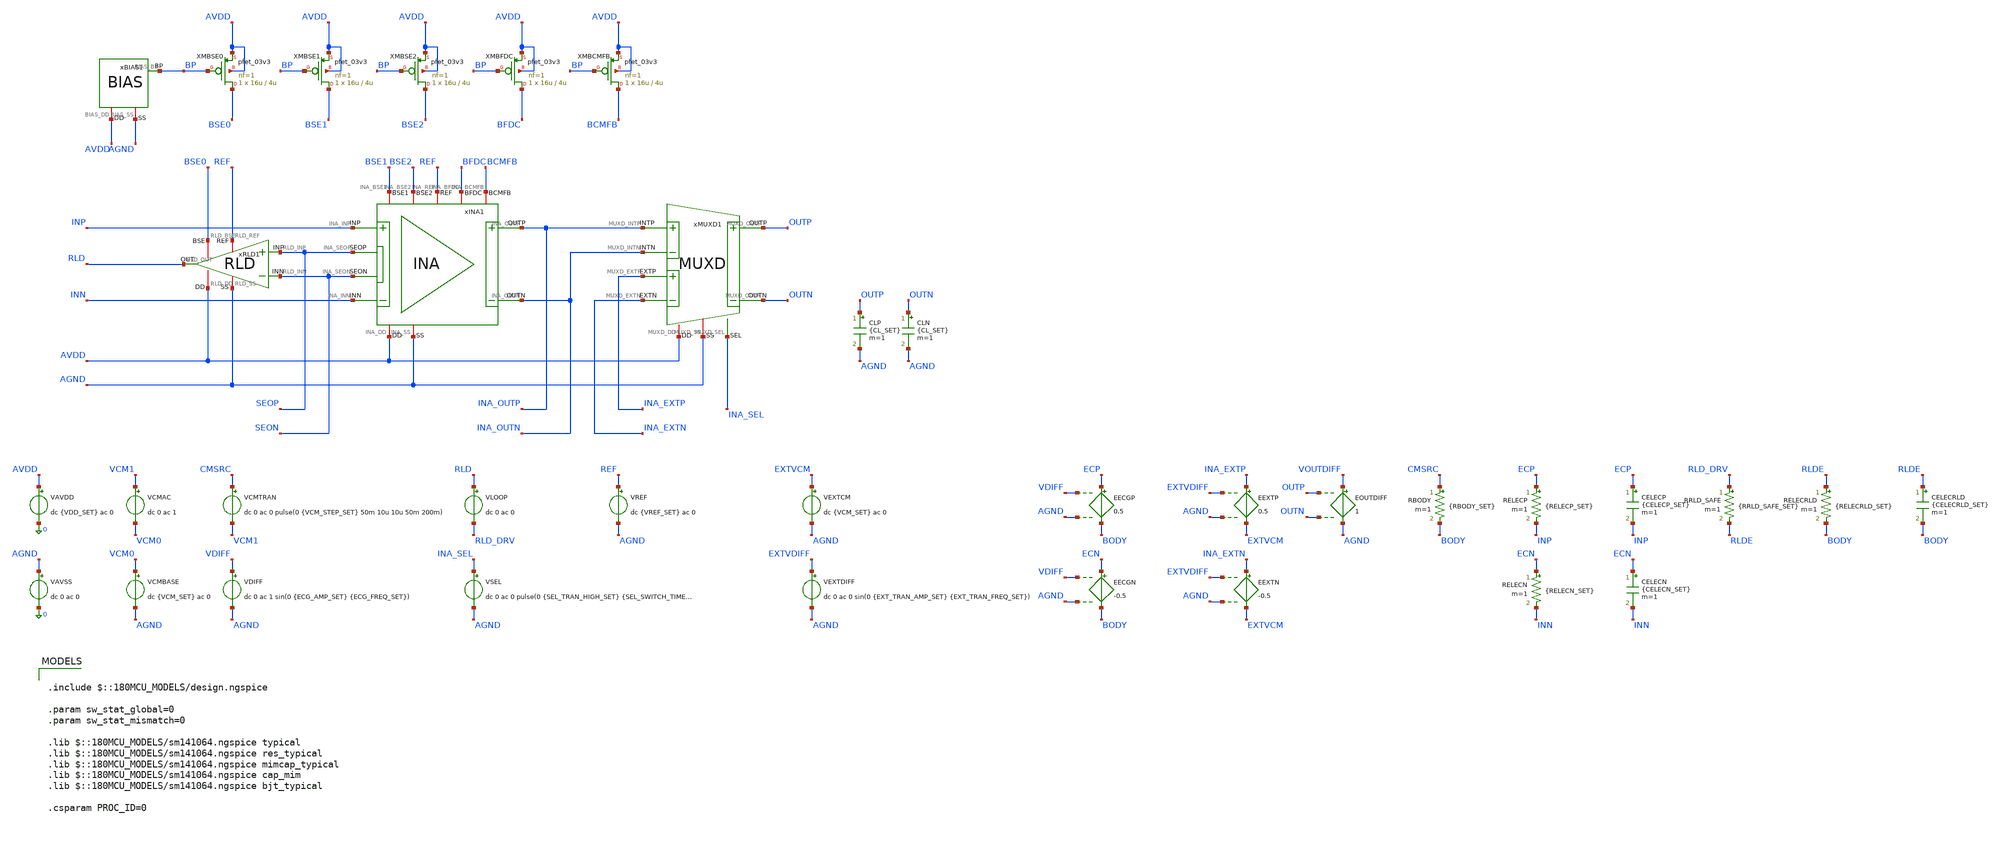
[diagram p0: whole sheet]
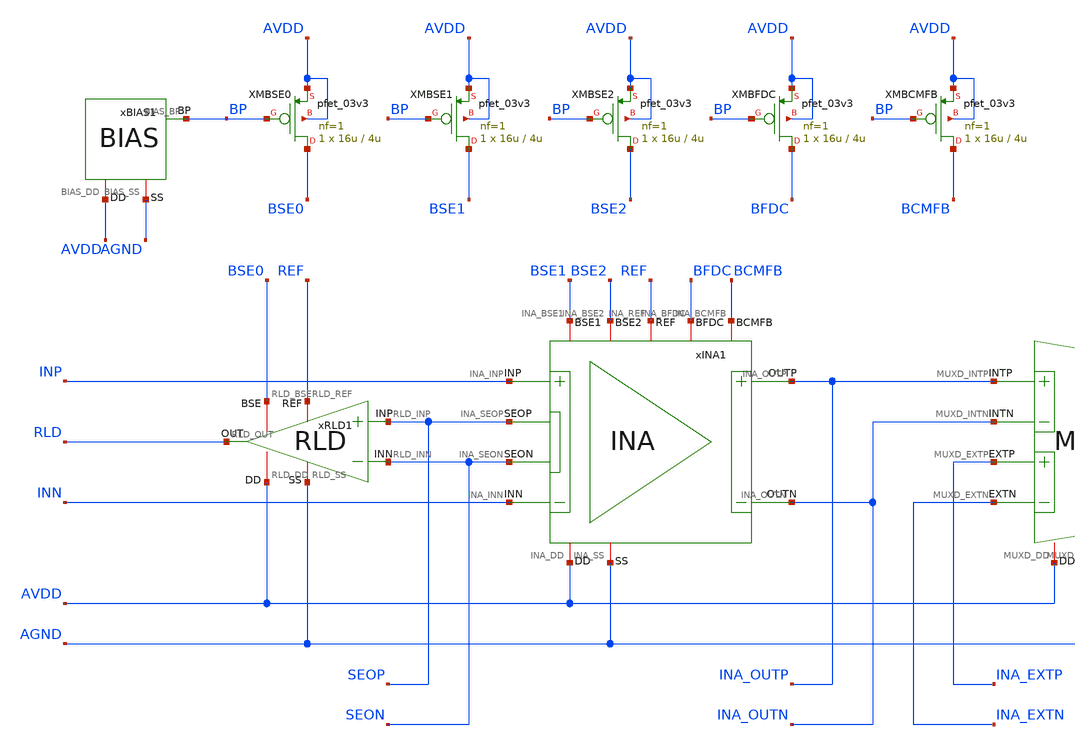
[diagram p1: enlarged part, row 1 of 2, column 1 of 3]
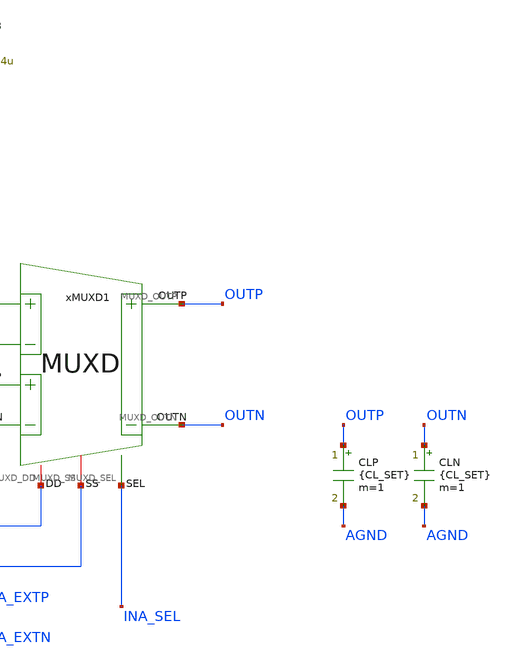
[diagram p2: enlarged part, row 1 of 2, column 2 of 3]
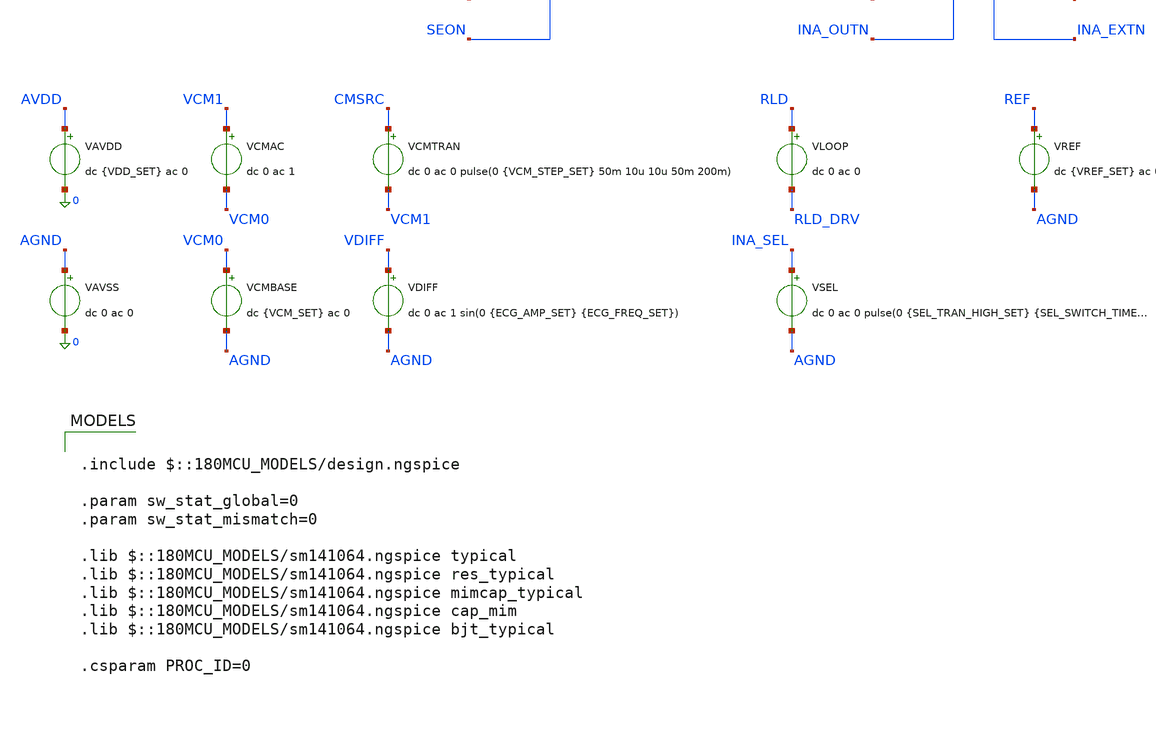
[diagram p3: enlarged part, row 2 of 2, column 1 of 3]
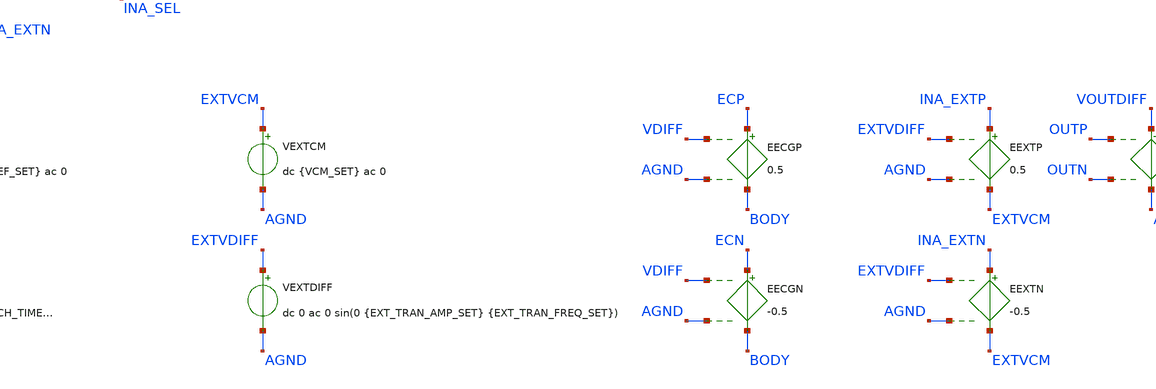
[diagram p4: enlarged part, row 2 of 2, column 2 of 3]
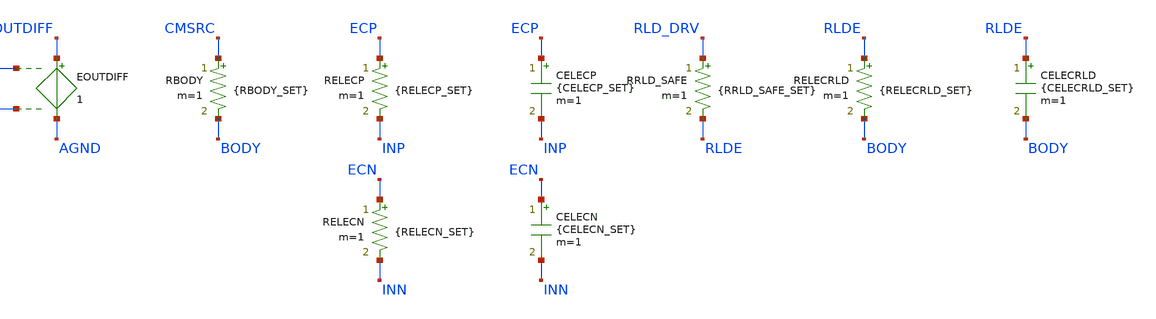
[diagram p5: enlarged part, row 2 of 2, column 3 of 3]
** sch_path: Design_Files/IC Design/Testbench/AFE_BLOCKS/INA_RLD/INA_RLD_TB_NOM.sch
**.subckt INA_RLD_TB_NOM
xMUXD1 AVDD AGND INA_OUTP INA_OUTN OUTN OUTP INA_EXTP INA_EXTN INA_SEL MUXD
xINA1 AVDD AGND INP INN INA_OUTN BFDC INA_OUTP BCMFB REF SEON SEOP BSE1 BSE2 INA
xRLD1 AVDD AGND SEOP SEON RLD REF BSE0 RLD
CLP OUTP AGND {CL_SET} m=1
CLN OUTN AGND {CL_SET} m=1
xBIAS1 AVDD AGND BP BIAS
XMBSE0 BSE0 BP AVDD AVDD pfet_03v3 L=4u W=16u nf=1 ad='int((nf+1)/2) * W/nf * 0.18u' as='int((nf+2)/2) * W/nf * 0.18u'
+ pd='2*int((nf+1)/2) * (W/nf + 0.18u)' ps='2*int((nf+2)/2) * (W/nf + 0.18u)' nrd='0.18u / W' nrs='0.18u / W'
+ sa=0 sb=0 sd=0 m=1
XMBSE1 BSE1 BP AVDD AVDD pfet_03v3 L=4u W=16u nf=1 ad='int((nf+1)/2) * W/nf * 0.18u' as='int((nf+2)/2) * W/nf * 0.18u'
+ pd='2*int((nf+1)/2) * (W/nf + 0.18u)' ps='2*int((nf+2)/2) * (W/nf + 0.18u)' nrd='0.18u / W' nrs='0.18u / W'
+ sa=0 sb=0 sd=0 m=1
XMBSE2 BSE2 BP AVDD AVDD pfet_03v3 L=4u W=16u nf=1 ad='int((nf+1)/2) * W/nf * 0.18u' as='int((nf+2)/2) * W/nf * 0.18u'
+ pd='2*int((nf+1)/2) * (W/nf + 0.18u)' ps='2*int((nf+2)/2) * (W/nf + 0.18u)' nrd='0.18u / W' nrs='0.18u / W'
+ sa=0 sb=0 sd=0 m=1
XMBFDC BFDC BP AVDD AVDD pfet_03v3 L=4u W=16u nf=1 ad='int((nf+1)/2) * W/nf * 0.18u' as='int((nf+2)/2) * W/nf * 0.18u'
+ pd='2*int((nf+1)/2) * (W/nf + 0.18u)' ps='2*int((nf+2)/2) * (W/nf + 0.18u)' nrd='0.18u / W' nrs='0.18u / W'
+ sa=0 sb=0 sd=0 m=1
XMBCMFB BCMFB BP AVDD AVDD pfet_03v3 L=4u W=16u nf=1 ad='int((nf+1)/2) * W/nf * 0.18u' as='int((nf+2)/2) * W/nf * 0.18u'
+ pd='2*int((nf+1)/2) * (W/nf + 0.18u)' ps='2*int((nf+2)/2) * (W/nf + 0.18u)' nrd='0.18u / W' nrs='0.18u / W'
+ sa=0 sb=0 sd=0 m=1
VAVDD AVDD 0 dc {VDD_SET} ac 0
.save i(vavdd)
VCMBASE VCM0 AGND dc {VCM_SET} ac 0
VCMAC VCM1 VCM0 dc 0 ac 1
VAVSS AGND 0 dc 0 ac 0
VCMTRAN CMSRC VCM1 dc 0 ac 0 pulse(0 {VCM_STEP_SET} 50m 10u 10u 50m 200m)
EECGP ECP BODY VDIFF AGND 0.5
EECGN ECN BODY VDIFF AGND -0.5
EEXTP INA_EXTP EXTVCM EXTVDIFF AGND 0.5
VDIFF VDIFF AGND dc 0 ac 1 sin(0 {ECG_AMP_SET} {ECG_FREQ_SET})
VLOOP RLD RLD_DRV dc 0 ac 0
.save i(vloop)
VSEL INA_SEL AGND dc 0 ac 0 pulse(0 {SEL_TRAN_HIGH_SET} {SEL_SWITCH_TIME_SET} 1u 1u 400m 800m)
VEXTCM EXTVCM AGND dc {VCM_SET} ac 0
VEXTDIFF EXTVDIFF AGND dc 0 ac 0 sin(0 {EXT_TRAN_AMP_SET} {EXT_TRAN_FREQ_SET})
EEXTN INA_EXTN EXTVCM EXTVDIFF AGND -0.5
EOUTDIFF VOUTDIFF AGND OUTP OUTN 1
RBODY CMSRC BODY {RBODY_SET} m=1
RELECP ECP INP {RELECP_SET} m=1
RELECN ECN INN {RELECN_SET} m=1
CELECP ECP INP {CELECP_SET} m=1
CELECN ECN INN {CELECN_SET} m=1
RRLD_SAFE RLD_DRV RLDE {RRLD_SAFE_SET} m=1
RELECRLD RLDE BODY {RELECRLD_SET} m=1
CELECRLD RLDE BODY {CELECRLD_SET} m=1
VREF REF AGND dc {VREF_SET} ac 0
.save i(vref)
**** begin user architecture code

.include $::180MCU_MODELS/design.ngspice

.param sw_stat_global=0
.param sw_stat_mismatch=0

.lib $::180MCU_MODELS/sm141064.ngspice typical
.lib $::180MCU_MODELS/sm141064.ngspice res_typical
.lib $::180MCU_MODELS/sm141064.ngspice mimcap_typical
.lib $::180MCU_MODELS/sm141064.ngspice cap_mim
.lib $::180MCU_MODELS/sm141064.ngspice bjt_typical

.csparam PROC_ID=0



.param VDD_SET=3.3
.param TEMP_SET=27
.param VCM_SET={VDD_SET/2}
.param VREF_SET={VDD_SET/2}

.param CL_SET=10p

.param ECG_AMP_SET=0.5m
.param ECG_FREQ_SET=10
.param VCM_STEP_SET=300m

.param RBODY_SET=100Meg

.param RELECP_SET=100k
.param RELECN_SET=100k
.param CELECP_SET=100n
.param CELECN_SET=100n

.param RRLD_SAFE_SET=1Meg
.param RELECRLD_SET=100k
.param CELECRLD_SET=100n

.param SEL_TRAN_HIGH_SET=0
.param SEL_SWITCH_TIME_SET=200m
.param EXT_TRAN_AMP_SET=0
.param EXT_TRAN_FREQ_SET=25

.csparam MC_RUNS=200

.temp {TEMP_SET}

.options gmin=1e-12
.options rshunt=1e12
.options method=gear





.control

destroy all

set noaskquit
set wr_singlescale
unset wr_vecnames

option klu
option numdgt=15
option method=gear
option maxord=2
option plotwinsize=0

if $&PROC_ID = 0
set proc=NOM
else
if $&PROC_ID = 1
set proc=FF
else
if $&PROC_ID = 2
set proc=SS
else
if $&PROC_ID = 3
set proc=FS
else
set proc=SF
end
end
end
end

shell mkdir -p /foss/designs/ECG_Acquisition_IC/Measurement_Results/IC_Simulation/AFE_BLOCKS/INA_RLD/{$proc}.Result_txt
shell rm -f /foss/designs/ECG_Acquisition_IC/Measurement_Results/IC_Simulation/AFE_BLOCKS/INA_RLD/{$proc}.Result_txt/{$proc}.*.txt

foreach vddval 3.3 3.0 3.6
foreach tval 27 -40 125

if $vddval = 3.3
if $tval = 27
set env=nom
else
if $tval = -40
set env=tl
else
set env=th
end
end
else
if $vddval = 3.0
if $tval = 27
set env=vl
else
if $tval = -40
set env=vltl
else
set env=vlth
end
end
else
if $tval = 27
set env=vh
else
if $tval = -40
set env=vhtl
else
set env=vhth
end
end
end
end

alterparam VDD_SET=$vddval
alterparam TEMP_SET=$tval

reset

save all
save @m.xmbse0.m0[id]
save @m.xmbse1.m0[id]
save @m.xmbse2.m0[id]
save @m.xmbfdc.m0[id]
save @m.xmbcmfb.m0[id]

foreach emode 0 1

if $emode = 0
set elec=bal
alter RELECP 100k
alter RELECN 100k
alter CELECP 100n
alter CELECN 100n
else
set elec=mis
alter RELECP 100k
alter RELECN 200k
alter CELECP 100n
alter CELECN 50n
end


* OFFSET

alter RRLD_SAFE 1Meg
alter @VSEL[DC]=0
alter @VDIFF[DC]=0

alter @VDIFF[ACMAG]=0
alter @VCMAC[ACMAG]=0
alter @VLOOP[ACMAG]=0
alter @VEXTDIFF[ACMAG]=0
alter @VREF[ACMAG]=0
alter @VAVDD[ACMAG]=0
alter @VAVSS[ACMAG]=0

dc VDIFF -10m 10m 10u

let ina_out_diff=v(INA_OUTP)-v(INA_OUTN)

meas dc vos_meas when ina_out_diff=0 cross=1

set vos_val=$&vos_meas

echo $vos_val > /foss/designs/ECG_Acquisition_IC/Measurement_Results/IC_Simulation/AFE_BLOCKS/INA_RLD/{$proc}.Result_txt/{$proc}.vos_{$env}_{$elec}.txt

destroy all

alter @VDIFF[DC]=$vos_val


* OP

alter RRLD_SAFE 1Meg
alter @VSEL[DC]=0

alter @VDIFF[ACMAG]=0
alter @VCMAC[ACMAG]=0
alter @VLOOP[ACMAG]=0
alter @VEXTDIFF[ACMAG]=0
alter @VREF[ACMAG]=0
alter @VAVDD[ACMAG]=0
alter @VAVSS[ACMAG]=0

op

let vin_cm=0.5*(v(INP)+v(INN))-v(AGND)
let vin_diff=v(INP)-v(INN)
let se_cm=0.5*(v(SEOP)+v(SEON))-v(AGND)
let se_diff=v(SEOP)-v(SEON)
let ina_out_cm=0.5*(v(INA_OUTP)+v(INA_OUTN))-v(AGND)
let ina_out_diff=v(INA_OUTP)-v(INA_OUTN)
let out_cm=0.5*(v(OUTP)+v(OUTN))-v(AGND)
let out_diff=v(OUTP)-v(OUTN)

let idd_total=abs(vavdd#branch)
let power_total=(v(AVDD)-v(AGND))*idd_total
let irld=abs(vloop#branch)

let ibse0=abs(@m.xmbse0.m0[id])
let ibse1=abs(@m.xmbse1.m0[id])
let ibse2=abs(@m.xmbse2.m0[id])
let ibfdc=abs(@m.xmbfdc.m0[id])
let ibcmfb=abs(@m.xmbcmfb.m0[id])

wrdata /foss/designs/ECG_Acquisition_IC/Measurement_Results/IC_Simulation/AFE_BLOCKS/INA_RLD/{$proc}.Result_txt/{$proc}.op_{$env}_{$elec}.txt
+ v(AVDD) v(REF) v(BP) vin_cm vin_diff v(SEOP) v(SEON) se_cm se_diff v(INA_OUTP) v(INA_OUTN) ina_out_cm
+ ina_out_diff v(OUTP) v(OUTN) out_cm out_diff v(RLD) v(BODY) irld idd_total power_total ibse0 ibse1 ibse2
+ ibfdc ibcmfb

destroy all


* INA AC

alter RRLD_SAFE 1Meg
alter @VSEL[DC]=0

alter @VDIFF[ACMAG]=1
alter @VDIFF[ACPHASE]=0
alter @VCMAC[ACMAG]=0
alter @VLOOP[ACMAG]=0
alter @VEXTDIFF[ACMAG]=0
alter @VREF[ACMAG]=0
alter @VAVDD[ACMAG]=0
alter @VAVSS[ACMAG]=0

ac dec 200 0.01 10Meg

let vin_diff=v(INP)-v(INN)
let se_diff=v(SEOP)-v(SEON)
let ina_out_diff=v(INA_OUTP)-v(INA_OUTN)
let out_diff=v(OUTP)-v(OUTN)

let vin_diff_real=real(vin_diff)
let vin_diff_imag=imag(vin_diff)

let se_diff_real=real(se_diff)
let se_diff_imag=imag(se_diff)

let ina_out_diff_real=real(ina_out_diff)
let ina_out_diff_imag=imag(ina_out_diff)

let out_diff_real=real(out_diff)
let out_diff_imag=imag(out_diff)

let rld_real=real(v(RLD))
let rld_imag=imag(v(RLD))

setscale frequency

wrdata /foss/designs/ECG_Acquisition_IC/Measurement_Results/IC_Simulation/AFE_BLOCKS/INA_RLD/{$proc}.Result_txt/{$proc}.diff_ac_{$env}_{$elec}.txt
+ vin_diff_real vin_diff_imag se_diff_real se_diff_imag ina_out_diff_real ina_out_diff_imag out_diff_real
+ out_diff_imag rld_real rld_imag

destroy all


* RLD OFF

alter RRLD_SAFE 1e15
alter @VSEL[DC]=0

alter @VDIFF[ACMAG]=0
alter @VCMAC[ACMAG]=1
alter @VCMAC[ACPHASE]=0
alter @VLOOP[ACMAG]=0
alter @VEXTDIFF[ACMAG]=0
alter @VREF[ACMAG]=0
alter @VAVDD[ACMAG]=0
alter @VAVSS[ACMAG]=0

ac dec 200 0.01 10Meg

let vcm_src=v(CMSRC)-v(AGND)
let body=v(BODY)-v(AGND)
let vin_cm=0.5*(v(INP)+v(INN))-v(AGND)
let se_cm=0.5*(v(SEOP)+v(SEON))-v(AGND)
let ina_out_diff=v(INA_OUTP)-v(INA_OUTN)
let out_diff=v(OUTP)-v(OUTN)

let vcm_src_real=real(vcm_src)
let vcm_src_imag=imag(vcm_src)

let body_real=real(body)
let body_imag=imag(body)

let vin_cm_real=real(vin_cm)
let vin_cm_imag=imag(vin_cm)

let se_cm_real=real(se_cm)
let se_cm_imag=imag(se_cm)

let ina_out_diff_real=real(ina_out_diff)
let ina_out_diff_imag=imag(ina_out_diff)

let out_diff_real=real(out_diff)
let out_diff_imag=imag(out_diff)

let rld_real=real(v(RLD))
let rld_imag=imag(v(RLD))

setscale frequency

wrdata /foss/designs/ECG_Acquisition_IC/Measurement_Results/IC_Simulation/AFE_BLOCKS/INA_RLD/{$proc}.Result_txt/{$proc}.cm_off_ac_{$env}_{$elec}.txt
+ vcm_src_real vcm_src_imag body_real body_imag vin_cm_real vin_cm_imag se_cm_real se_cm_imag out_diff_real
+ out_diff_imag rld_real rld_imag

wrdata /foss/designs/ECG_Acquisition_IC/Measurement_Results/IC_Simulation/AFE_BLOCKS/INA_RLD/{$proc}.Result_txt/{$proc}.ina_cmrr_ac_{$env}_{$elec}.txt
+ vin_cm_real vin_cm_imag ina_out_diff_real ina_out_diff_imag

destroy all


* RLD ON

alter RRLD_SAFE 1Meg
alter @VSEL[DC]=0

alter @VDIFF[ACMAG]=0
alter @VCMAC[ACMAG]=1
alter @VCMAC[ACPHASE]=0
alter @VLOOP[ACMAG]=0
alter @VEXTDIFF[ACMAG]=0
alter @VREF[ACMAG]=0
alter @VAVDD[ACMAG]=0
alter @VAVSS[ACMAG]=0

ac dec 200 0.01 10Meg

let vcm_src=v(CMSRC)-v(AGND)
let body=v(BODY)-v(AGND)
let vin_cm=0.5*(v(INP)+v(INN))-v(AGND)
let se_cm=0.5*(v(SEOP)+v(SEON))-v(AGND)
let out_diff=v(OUTP)-v(OUTN)

let vcm_src_real=real(vcm_src)
let vcm_src_imag=imag(vcm_src)

let body_real=real(body)
let body_imag=imag(body)

let vin_cm_real=real(vin_cm)
let vin_cm_imag=imag(vin_cm)

let se_cm_real=real(se_cm)
let se_cm_imag=imag(se_cm)

let out_diff_real=real(out_diff)
let out_diff_imag=imag(out_diff)

let rld_real=real(v(RLD))
let rld_imag=imag(v(RLD))

setscale frequency

wrdata /foss/designs/ECG_Acquisition_IC/Measurement_Results/IC_Simulation/AFE_BLOCKS/INA_RLD/{$proc}.Result_txt/{$proc}.cm_on_ac_{$env}_{$elec}.txt
+ vcm_src_real vcm_src_imag body_real body_imag vin_cm_real vin_cm_imag se_cm_real se_cm_imag out_diff_real
+ out_diff_imag rld_real rld_imag

destroy all


* PSRR+

alter RRLD_SAFE 1Meg
alter @VSEL[DC]=0

alter @VDIFF[ACMAG]=0
alter @VCMAC[ACMAG]=0
alter @VLOOP[ACMAG]=0
alter @VEXTDIFF[ACMAG]=0
alter @VREF[ACMAG]=0

alter @VAVDD[ACMAG]=1
alter @VAVDD[ACPHASE]=0
alter @VAVSS[ACMAG]=0

ac dec 200 0.01 10Meg

let vsup=v(AVDD)-v(AGND)
let ina_out_diff=v(INA_OUTP)-v(INA_OUTN)
let out_diff=v(OUTP)-v(OUTN)

let vsup_real=real(vsup)
let vsup_imag=imag(vsup)

let ina_out_diff_real=real(ina_out_diff)
let ina_out_diff_imag=imag(ina_out_diff)

let out_diff_real=real(out_diff)
let out_diff_imag=imag(out_diff)

setscale frequency

wrdata /foss/designs/ECG_Acquisition_IC/Measurement_Results/IC_Simulation/AFE_BLOCKS/INA_RLD/{$proc}.Result_txt/{$proc}.psrrp_ac_{$env}_{$elec}.txt
+ vsup_real vsup_imag ina_out_diff_real ina_out_diff_imag out_diff_real out_diff_imag

destroy all


* PSRR-

alter RRLD_SAFE 1Meg
alter @VSEL[DC]=0

alter @VDIFF[ACMAG]=0
alter @VCMAC[ACMAG]=0
alter @VLOOP[ACMAG]=0
alter @VEXTDIFF[ACMAG]=0
alter @VREF[ACMAG]=0

alter @VAVDD[ACMAG]=0
alter @VAVSS[ACMAG]=1
alter @VAVSS[ACPHASE]=0

ac dec 200 0.01 10Meg

let vsup=v(AVDD)-v(AGND)
let ina_out_diff=v(INA_OUTP)-v(INA_OUTN)
let out_diff=v(OUTP)-v(OUTN)

let vsup_real=real(vsup)
let vsup_imag=imag(vsup)

let ina_out_diff_real=real(ina_out_diff)
let ina_out_diff_imag=imag(ina_out_diff)

let out_diff_real=real(out_diff)
let out_diff_imag=imag(out_diff)

setscale frequency

wrdata /foss/designs/ECG_Acquisition_IC/Measurement_Results/IC_Simulation/AFE_BLOCKS/INA_RLD/{$proc}.Result_txt/{$proc}.psrrn_ac_{$env}_{$elec}.txt
+ vsup_real vsup_imag ina_out_diff_real ina_out_diff_imag out_diff_real out_diff_imag

destroy all


* RLD LOOP

alter RRLD_SAFE 1Meg
alter @VSEL[DC]=0

alter @VDIFF[ACMAG]=0
alter @VCMAC[ACMAG]=0
alter @VLOOP[ACMAG]=1
alter @VLOOP[ACPHASE]=0
alter @VEXTDIFF[ACMAG]=0
alter @VREF[ACMAG]=0
alter @VAVDD[ACMAG]=0
alter @VAVSS[ACMAG]=0

ac dec 200 0.01 10Meg

let loop_in=v(RLD_DRV)-v(AGND)
let loop_out=v(RLD)-v(AGND)
let body=v(BODY)-v(AGND)
let vin_cm=0.5*(v(INP)+v(INN))-v(AGND)
let se_cm=0.5*(v(SEOP)+v(SEON))-v(AGND)

let loop_in_real=real(loop_in)
let loop_in_imag=imag(loop_in)

let loop_out_real=real(loop_out)
let loop_out_imag=imag(loop_out)

let body_real=real(body)
let body_imag=imag(body)

let vin_cm_real=real(vin_cm)
let vin_cm_imag=imag(vin_cm)

let se_cm_real=real(se_cm)
let se_cm_imag=imag(se_cm)

setscale frequency

wrdata /foss/designs/ECG_Acquisition_IC/Measurement_Results/IC_Simulation/AFE_BLOCKS/INA_RLD/{$proc}.Result_txt/{$proc}.rld_loop_ac_{$env}_{$elec}.txt
+ loop_in_real loop_in_imag loop_out_real loop_out_imag body_real body_imag vin_cm_real vin_cm_imag se_cm_real
+ se_cm_imag

destroy all


* NOISE

alter RRLD_SAFE 1Meg
alter @VSEL[DC]=0

alter @VDIFF[ACMAG]=1
alter @VDIFF[ACPHASE]=0
alter @VCMAC[ACMAG]=0
alter @VLOOP[ACMAG]=0
alter @VEXTDIFF[ACMAG]=0
alter @VREF[ACMAG]=0
alter @VAVDD[ACMAG]=0
alter @VAVSS[ACMAG]=0

option sparse

noise v(VOUTDIFF) VDIFF dec 100 0.01 1k

setplot previous
setscale frequency

wrdata /foss/designs/ECG_Acquisition_IC/Measurement_Results/IC_Simulation/AFE_BLOCKS/INA_RLD/{$proc}.Result_txt/{$proc}.noise_{$env}_{$elec}.txt
+ onoise_spectrum inoise_spectrum

destroy all


* CM TRAN

alter RRLD_SAFE 1Meg
alter @VSEL[DC]=0

alter @VDIFF[ACMAG]=0
alter @VCMAC[ACMAG]=0
alter @VLOOP[ACMAG]=0
alter @VEXTDIFF[ACMAG]=0
alter @VREF[ACMAG]=0
alter @VAVDD[ACMAG]=0
alter @VAVSS[ACMAG]=0

tran 10u 200m

let vin_cm=0.5*(v(INP)+v(INN))-v(AGND)
let vin_diff=v(INP)-v(INN)

let se_cm=0.5*(v(SEOP)+v(SEON))-v(AGND)
let se_diff=v(SEOP)-v(SEON)

let ina_out_cm=0.5*(v(INA_OUTP)+v(INA_OUTN))-v(AGND)
let ina_out_diff=v(INA_OUTP)-v(INA_OUTN)

let out_cm=0.5*(v(OUTP)+v(OUTN))-v(AGND)
let out_diff=v(OUTP)-v(OUTN)

let irld=abs(vloop#branch)
let idd_total=abs(vavdd#branch)

wrdata /foss/designs/ECG_Acquisition_IC/Measurement_Results/IC_Simulation/AFE_BLOCKS/INA_RLD/{$proc}.Result_txt/{$proc}.tran_{$env}_{$elec}.txt
+ v(CMSRC) v(BODY) vin_cm vin_diff v(SEOP) v(SEON) se_cm se_diff v(INA_OUTP) v(INA_OUTN) ina_out_cm ina_out_diff
+ v(RLD) v(OUTP) v(OUTN) out_cm out_diff irld idd_total

destroy all

end

end
end


* SEL NOM

if $&PROC_ID = 0

alterparam VDD_SET=3.3
alterparam TEMP_SET=27
alterparam VCM_STEP_SET=0
alterparam SEL_TRAN_HIGH_SET=3.3
alterparam EXT_TRAN_AMP_SET=50m
alterparam EXT_TRAN_FREQ_SET=25

reset
save all

alter RELECP 100k
alter RELECN 100k
alter CELECP 100n
alter CELECN 100n
alter RRLD_SAFE 1Meg

alter @VDIFF[DC]=0
alter @VDIFF[ACMAG]=0
alter @VCMAC[ACMAG]=0
alter @VLOOP[ACMAG]=0
alter @VEXTDIFF[ACMAG]=0
alter @VREF[ACMAG]=0
alter @VAVDD[ACMAG]=0
alter @VAVSS[ACMAG]=0

tran 10u 400m

let ina_out_diff=v(INA_OUTP)-v(INA_OUTN)
let ext_in_diff=v(INA_EXTP)-v(INA_EXTN)
let out_diff=v(OUTP)-v(OUTN)

wrdata /foss/designs/ECG_Acquisition_IC/Measurement_Results/IC_Simulation/AFE_BLOCKS/INA_RLD/{$proc}.Result_txt/{$proc}.sel_tran_nom.txt
+ v(INA_SEL) ina_out_diff ext_in_diff out_diff

destroy all

end

quit

.endc


**** end user architecture code
**.ends
.end
